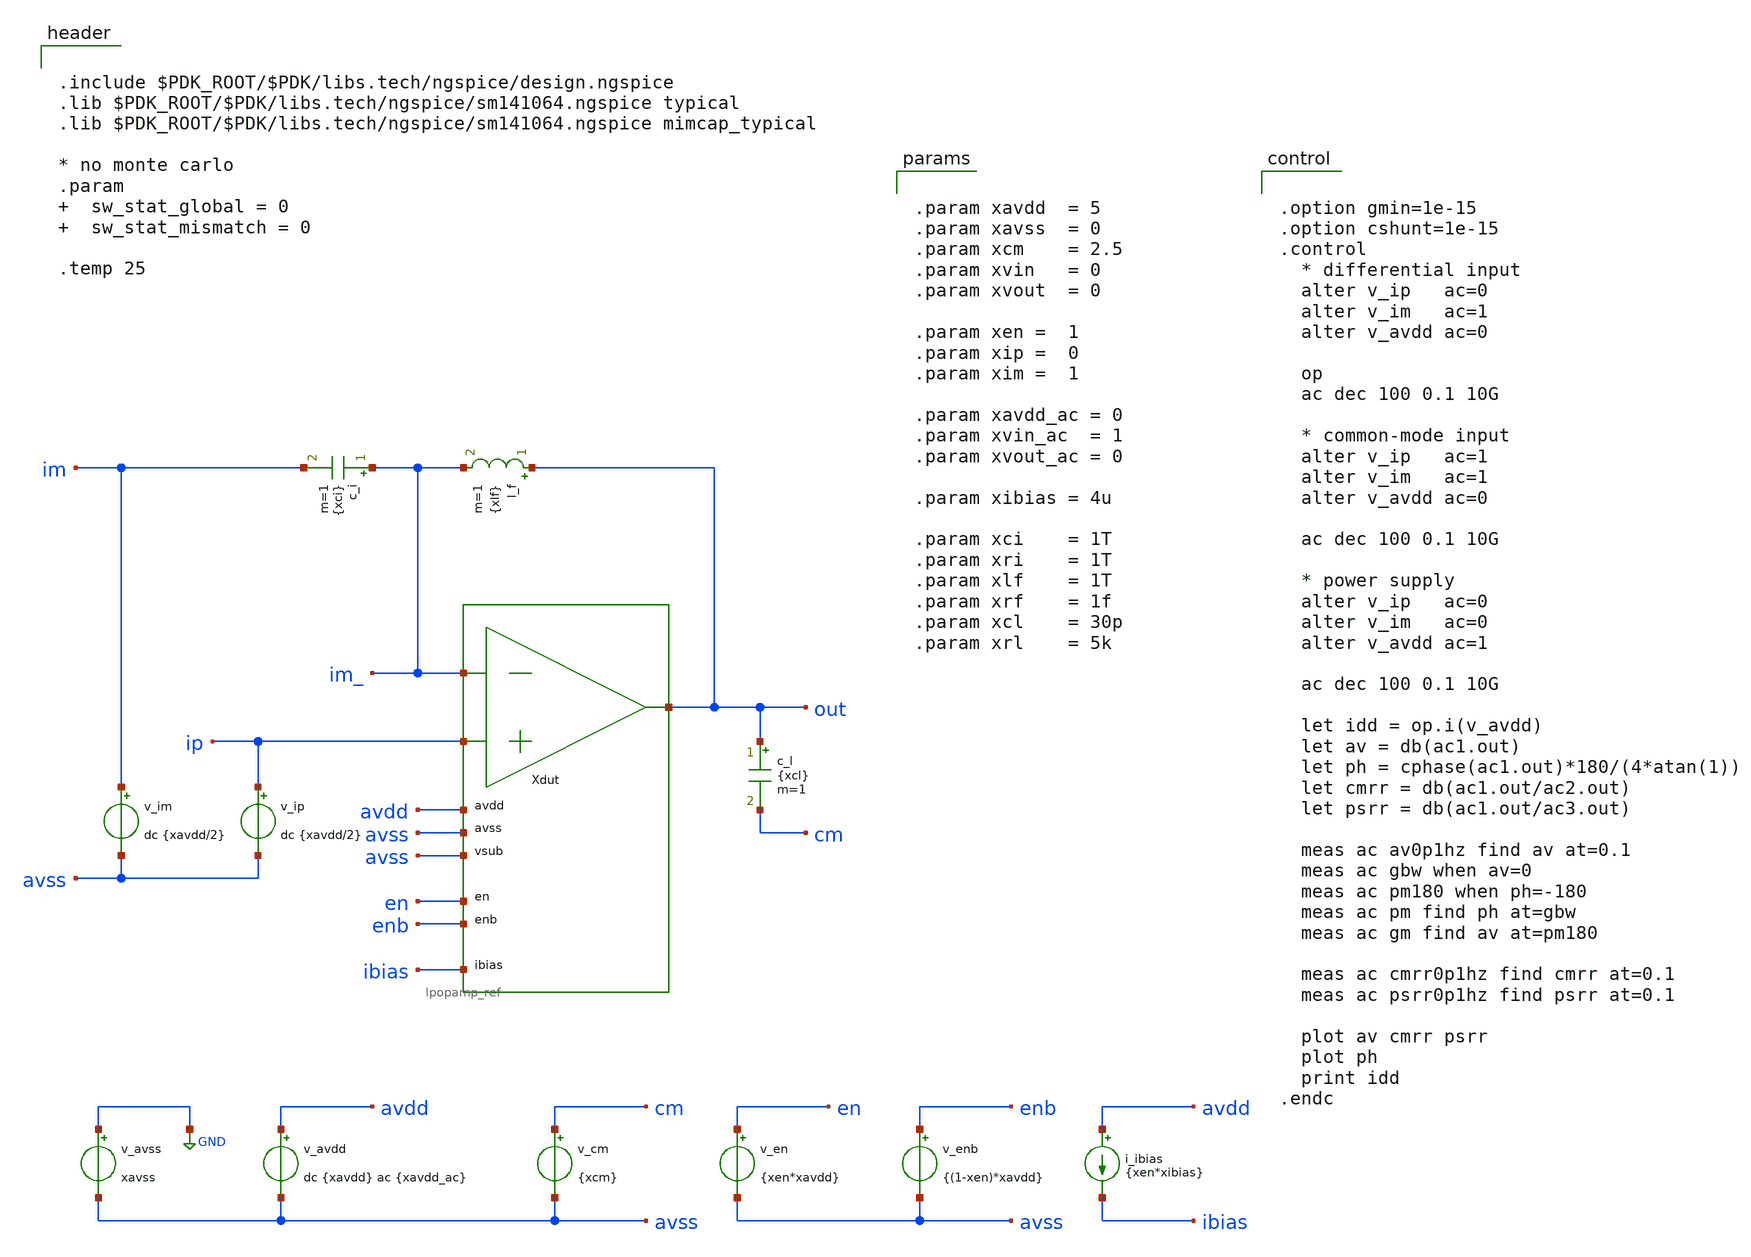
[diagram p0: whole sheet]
** sch_path: xschem/tb_lpopamp_open_ac.sch
**.subckt tb_lpopamp_open_ac
Xdut im_ ip out avdd avss avss en enb ibias lpopamp_ref
v_avss GND avss xavss
v_avdd avdd avss dc {xavdd} ac {xavdd_ac}
v_en en avss {xen*xavdd}
v_enb enb avss {(1-xen)*xavdd}
i_ibias avdd ibias {xen*xibias}
c_l out cm {xcl} m=1
c_i im_ im {xci} m=1
l_f out im_ {xlf} m=1
v_cm cm avss {xcm}
v_im im avss dc {xavdd/2}
v_ip ip avss dc {xavdd/2}
**** begin user architecture code


.include $PDK_ROOT/$PDK/libs.tech/ngspice/design.ngspice
.lib $PDK_ROOT/$PDK/libs.tech/ngspice/sm141064.ngspice typical
.lib $PDK_ROOT/$PDK/libs.tech/ngspice/sm141064.ngspice mimcap_typical

* no monte carlo
.param   sw_stat_global = 0   sw_stat_mismatch = 0

.temp 25




.option gmin=1e-15
.option cshunt=1e-15
.control
  * differential input
  alter v_ip   ac=0
  alter v_im   ac=1
  alter v_avdd ac=0

  op
  ac dec 100 0.1 10G

  * common-mode input
  alter v_ip   ac=1
  alter v_im   ac=1
  alter v_avdd ac=0

  ac dec 100 0.1 10G

  * power supply
  alter v_ip   ac=0
  alter v_im   ac=0
  alter v_avdd ac=1

  ac dec 100 0.1 10G

  let idd = op.i(v_avdd)
  let av = db(ac1.out)
  let ph = cphase(ac1.out)*180/(4*atan(1))
  let cmrr = db(ac1.out/ac2.out)
  let psrr = db(ac1.out/ac3.out)

  meas ac av0p1hz find av at=0.1
  meas ac gbw when av=0
  meas ac pm180 when ph=-180
  meas ac pm find ph at=gbw
  meas ac gm find av at=pm180

  meas ac cmrr0p1hz find cmrr at=0.1
  meas ac psrr0p1hz find psrr at=0.1

  plot av cmrr psrr
  plot ph
  print idd
.endc




.param xavdd  = 5
.param xavss  = 0
.param xcm    = 2.5
.param xvin   = 0
.param xvout  = 0

.param xen =  1
.param xip =  0
.param xim =  1

.param xavdd_ac = 0
.param xvin_ac  = 1
.param xvout_ac = 0

.param xibias = 4u

.param xci    = 1T
.param xri    = 1T
.param xlf    = 1T
.param xrf    = 1f
.param xcl    = 30p
.param xrl    = 5k


**** end user architecture code
**.ends
.GLOBAL GND
.end
